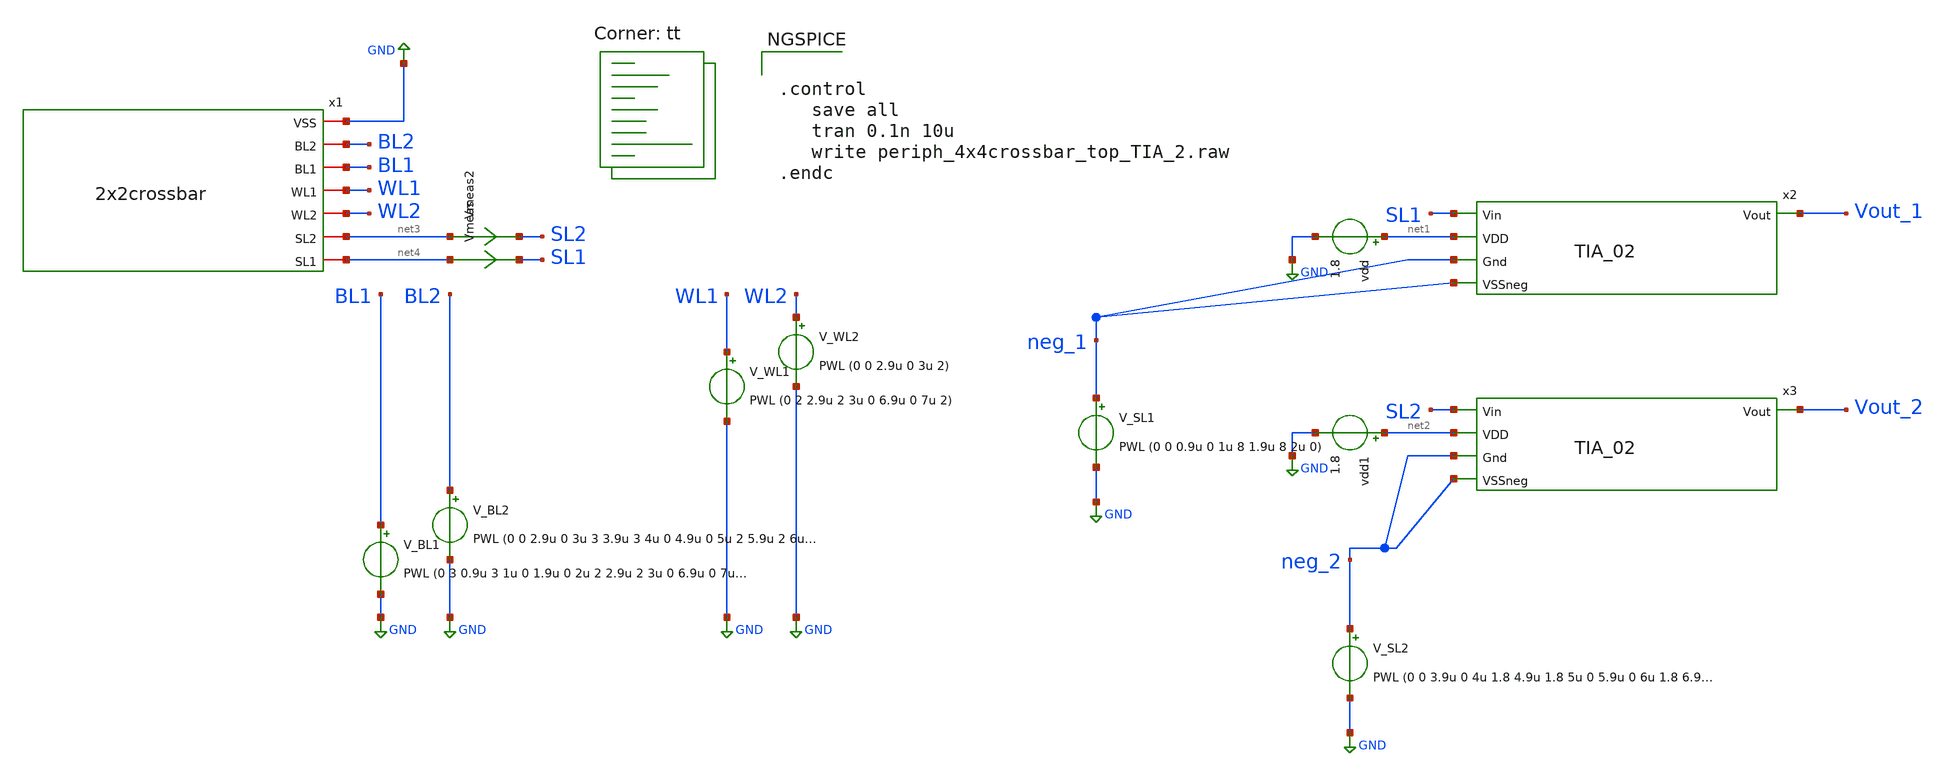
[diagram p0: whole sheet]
** sch_path: xschem/test/xschem/periph_4x4crossbar_top_TIA_2.sch
**.subckt periph_4x4crossbar_top_TIA_2
x2 SL1 net1 Vout_1 neg_1 neg_1 TIA_02
vdd net1 GND 1.8
x3 SL2 net2 Vout_2 neg_2 neg_2 TIA_02
vdd1 net2 GND 1.8
V_BL1 BL1 GND PWL (0 3 0.9u 3 1u 0 1.9u 0 2u 2 2.9u 2 3u 0 6.9u 0 7u 0.2)
V_BL2 BL2 GND PWL (0 0 2.9u 0 3u 3 3.9u 3 4u 0 4.9u 0 5u 2 5.9u 2 6u 0 6.9u 0 7u 0.2)
x1 GND BL2 BL1 WL1 WL2 net3 net4 2x2crossbar
V_SL1 neg_1 GND PWL (0 0 0.9u 0 1u 8 1.9u 8 2u 0)
V_SL2 neg_2 GND PWL (0 0 3.9u 0 4u 1.8 4.9u 1.8 5u 0 5.9u 0 6u 1.8 6.9u 1.8 7u 0)
V_WL1 WL1 GND PWL (0 2 2.9u 2 3u 0 6.9u 0 7u 2)
V_WL2 WL2 GND PWL (0 0 2.9u 0 3u 2)
Vmeas2 net3 SL2 0
.save i(vmeas2)
Vmeas net4 SL1 0
.save i(vmeas)
**** begin user architecture code
.lib $::SKYWATER_MODELS/sky130.lib.spice tt


.control
   save all
   tran 0.1n 10u
   write periph_4x4crossbar_top_TIA_2.raw
.endc


**** end user architecture code
**.ends
.GLOBAL GND
.end
